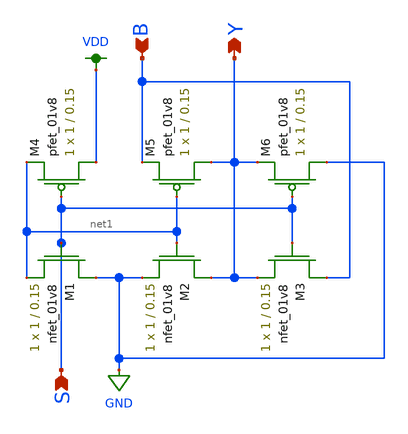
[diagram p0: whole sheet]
** sch_path: dac/schematics/mux_lds.sch
**.subckt mux_lds S B Y
*.ipin S
*.ipin B
*.opin Y
XM1 GND S net1 GND sky130_fd_pr__nfet_01v8 L=0.15 W=1 nf=1 ad='int((nf+1)/2) * W/nf * 0.29' as='int((nf+2)/2) * W/nf * 0.29'
+ pd='2*int((nf+1)/2) * (W/nf + 0.29)' ps='2*int((nf+2)/2) * (W/nf + 0.29)' nrd='0.29 / W' nrs='0.29 / W'
+ sa=0 sb=0 sd=0 mult=1 m=1
XM2 Y net1 GND GND sky130_fd_pr__nfet_01v8 L=0.15 W=1 nf=1 ad='int((nf+1)/2) * W/nf * 0.29' as='int((nf+2)/2) * W/nf * 0.29'
+ pd='2*int((nf+1)/2) * (W/nf + 0.29)' ps='2*int((nf+2)/2) * (W/nf + 0.29)' nrd='0.29 / W' nrs='0.29 / W'
+ sa=0 sb=0 sd=0 mult=1 m=1
XM3 B S Y GND sky130_fd_pr__nfet_01v8 L=0.15 W=1 nf=1 ad='int((nf+1)/2) * W/nf * 0.29' as='int((nf+2)/2) * W/nf * 0.29'
+ pd='2*int((nf+1)/2) * (W/nf + 0.29)' ps='2*int((nf+2)/2) * (W/nf + 0.29)' nrd='0.29 / W' nrs='0.29 / W'
+ sa=0 sb=0 sd=0 mult=1 m=1
XM4 VDD S net1 VDD sky130_fd_pr__pfet_01v8 L=0.15 W=1 nf=1 ad='int((nf+1)/2) * W/nf * 0.29' as='int((nf+2)/2) * W/nf * 0.29'
+ pd='2*int((nf+1)/2) * (W/nf + 0.29)' ps='2*int((nf+2)/2) * (W/nf + 0.29)' nrd='0.29 / W' nrs='0.29 / W'
+ sa=0 sb=0 sd=0 mult=1 m=1
XM5 Y net1 B VDD sky130_fd_pr__pfet_01v8 L=0.15 W=1 nf=1 ad='int((nf+1)/2) * W/nf * 0.29' as='int((nf+2)/2) * W/nf * 0.29'
+ pd='2*int((nf+1)/2) * (W/nf + 0.29)' ps='2*int((nf+2)/2) * (W/nf + 0.29)' nrd='0.29 / W' nrs='0.29 / W'
+ sa=0 sb=0 sd=0 mult=1 m=1
XM6 GND S Y VDD sky130_fd_pr__pfet_01v8 L=0.15 W=1 nf=1 ad='int((nf+1)/2) * W/nf * 0.29' as='int((nf+2)/2) * W/nf * 0.29'
+ pd='2*int((nf+1)/2) * (W/nf + 0.29)' ps='2*int((nf+2)/2) * (W/nf + 0.29)' nrd='0.29 / W' nrs='0.29 / W'
+ sa=0 sb=0 sd=0 mult=1 m=1
**.ends
.GLOBAL GND
.GLOBAL VDD
.end
